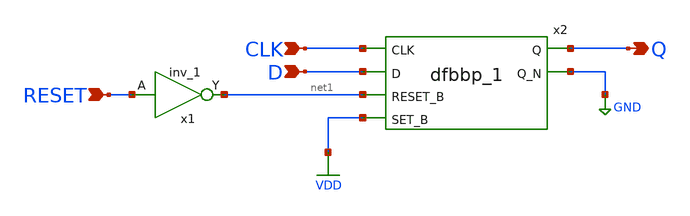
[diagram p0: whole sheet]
** sch_path: my_df.sch
**.subckt my_df CLK D RESET Q
*.ipin CLK
*.ipin D
*.ipin RESET
*.opin Q
x1 RESET GND GND VDD VDD net1 sky130_fd_sc_hd__inv_1
x2 CLK D net1 VDD GND GND VDD VDD Q GND sky130_fd_sc_hd__dfbbp_1
**.ends
.GLOBAL VDD
.GLOBAL GND
.end
